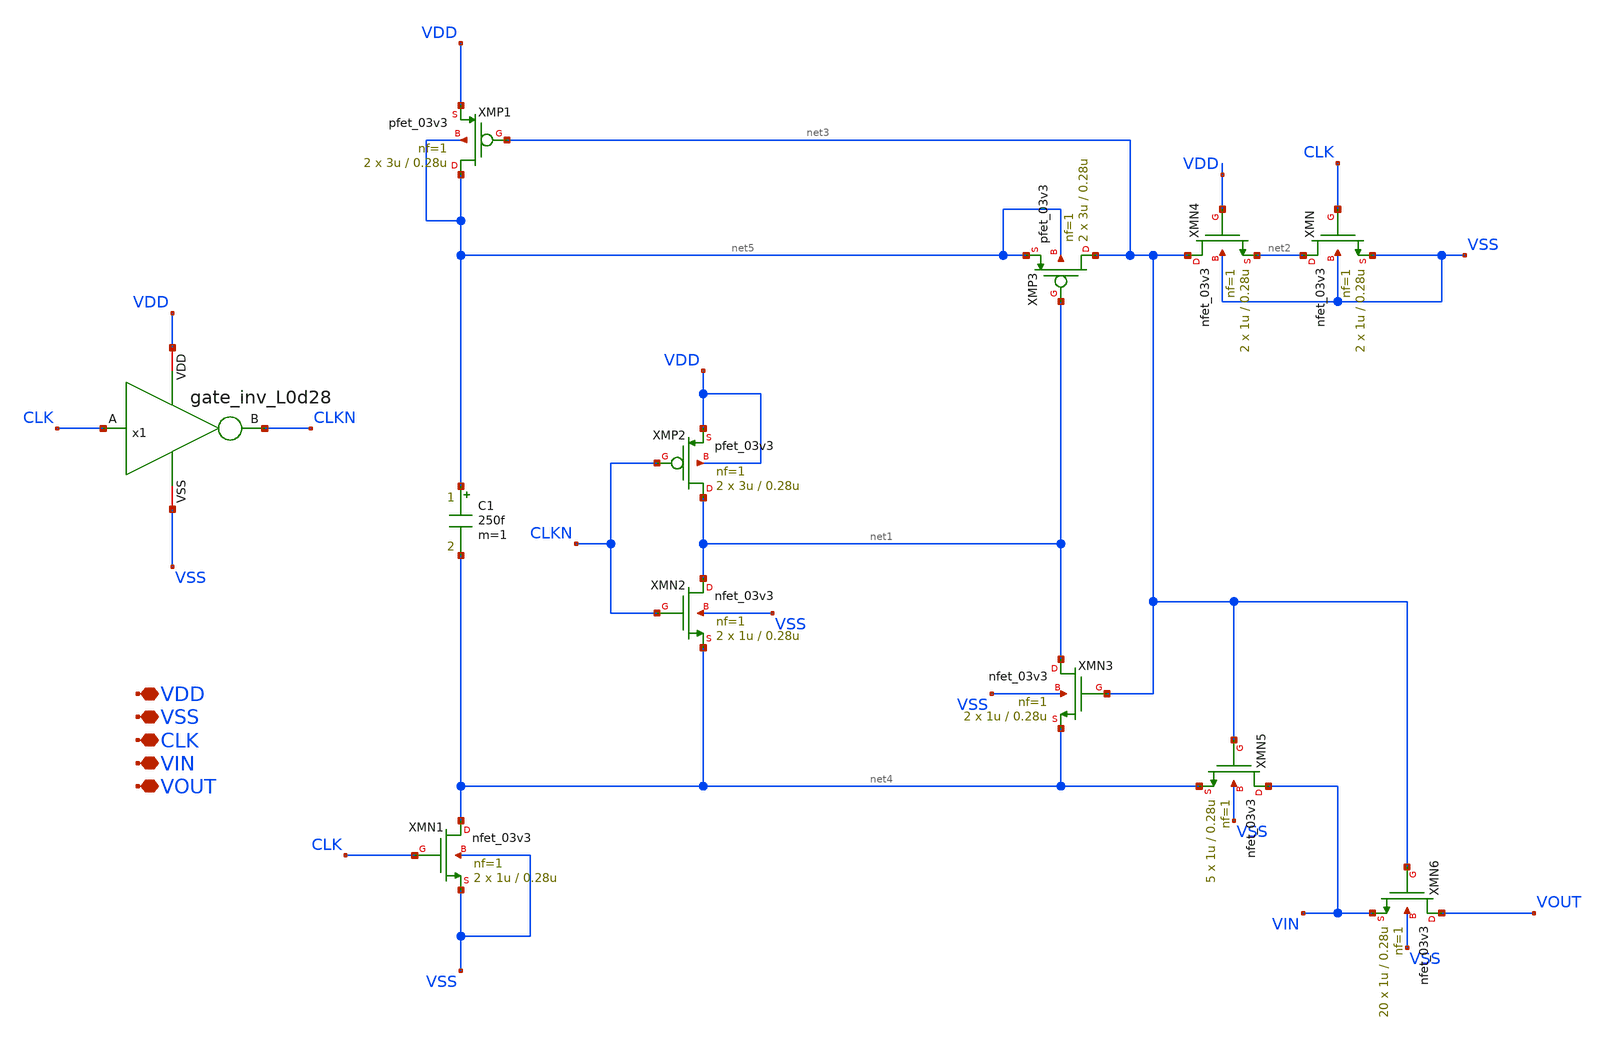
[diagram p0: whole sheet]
** sch_path: designs/sar_adc/samplehold/samplehold/xschem/samplehold.sch
**.subckt samplehold CLK VSS VDD VOUT VIN
*.iopin CLK
*.iopin VSS
*.iopin VDD
*.iopin VOUT
*.iopin VIN
C1 net5 net4 250f m=1
XMN net2 CLK VSS VSS nfet_03v3 L=0.28u W=1u nf=1 ad='int((nf+1)/2) * W/nf * 0.18u' as='int((nf+2)/2) * W/nf * 0.18u'
+ pd='2*int((nf+1)/2) * (W/nf + 0.18u)' ps='2*int((nf+2)/2) * (W/nf + 0.18u)' nrd='0.18u / W' nrs='0.18u / W'
+ sa=0 sb=0 sd=0 m=2
XMP1 net5 net3 VDD net5 pfet_03v3 L=0.28u W=3u nf=1 ad='int((nf+1)/2) * W/nf * 0.18u' as='int((nf+2)/2) * W/nf * 0.18u'
+ pd='2*int((nf+1)/2) * (W/nf + 0.18u)' ps='2*int((nf+2)/2) * (W/nf + 0.18u)' nrd='0.18u / W' nrs='0.18u / W'
+ sa=0 sb=0 sd=0 m=2
XMN1 net4 CLK VSS VSS nfet_03v3 L=0.28u W=1u nf=1 ad='int((nf+1)/2) * W/nf * 0.18u' as='int((nf+2)/2) * W/nf * 0.18u'
+ pd='2*int((nf+1)/2) * (W/nf + 0.18u)' ps='2*int((nf+2)/2) * (W/nf + 0.18u)' nrd='0.18u / W' nrs='0.18u / W'
+ sa=0 sb=0 sd=0 m=2
XMP2 net1 CLKN VDD VDD pfet_03v3 L=0.28u W=3u nf=1 ad='int((nf+1)/2) * W/nf * 0.18u' as='int((nf+2)/2) * W/nf * 0.18u'
+ pd='2*int((nf+1)/2) * (W/nf + 0.18u)' ps='2*int((nf+2)/2) * (W/nf + 0.18u)' nrd='0.18u / W' nrs='0.18u / W'
+ sa=0 sb=0 sd=0 m=2
XMN2 net1 CLKN net4 VSS nfet_03v3 L=0.28u W=1u nf=1 ad='int((nf+1)/2) * W/nf * 0.18u' as='int((nf+2)/2) * W/nf * 0.18u'
+ pd='2*int((nf+1)/2) * (W/nf + 0.18u)' ps='2*int((nf+2)/2) * (W/nf + 0.18u)' nrd='0.18u / W' nrs='0.18u / W'
+ sa=0 sb=0 sd=0 m=2
XMN3 net1 net3 net4 VSS nfet_03v3 L=0.28u W=1u nf=1 ad='int((nf+1)/2) * W/nf * 0.18u' as='int((nf+2)/2) * W/nf * 0.18u'
+ pd='2*int((nf+1)/2) * (W/nf + 0.18u)' ps='2*int((nf+2)/2) * (W/nf + 0.18u)' nrd='0.18u / W' nrs='0.18u / W'
+ sa=0 sb=0 sd=0 m=2
XMP3 net3 net1 net5 net5 pfet_03v3 L=0.28u W=3u nf=1 ad='int((nf+1)/2) * W/nf * 0.18u' as='int((nf+2)/2) * W/nf * 0.18u'
+ pd='2*int((nf+1)/2) * (W/nf + 0.18u)' ps='2*int((nf+2)/2) * (W/nf + 0.18u)' nrd='0.18u / W' nrs='0.18u / W'
+ sa=0 sb=0 sd=0 m=2
XMN4 net3 VDD net2 VSS nfet_03v3 L=0.28u W=1u nf=1 ad='int((nf+1)/2) * W/nf * 0.18u' as='int((nf+2)/2) * W/nf * 0.18u'
+ pd='2*int((nf+1)/2) * (W/nf + 0.18u)' ps='2*int((nf+2)/2) * (W/nf + 0.18u)' nrd='0.18u / W' nrs='0.18u / W'
+ sa=0 sb=0 sd=0 m=2
XMN5 VIN net3 net4 VSS nfet_03v3 L=0.28u W=1u nf=1 ad='int((nf+1)/2) * W/nf * 0.18u' as='int((nf+2)/2) * W/nf * 0.18u'
+ pd='2*int((nf+1)/2) * (W/nf + 0.18u)' ps='2*int((nf+2)/2) * (W/nf + 0.18u)' nrd='0.18u / W' nrs='0.18u / W'
+ sa=0 sb=0 sd=0 m=5
XMN6 VOUT net3 VIN VSS nfet_03v3 L=0.28u W=1u nf=1 ad='int((nf+1)/2) * W/nf * 0.18u' as='int((nf+2)/2) * W/nf * 0.18u'
+ pd='2*int((nf+1)/2) * (W/nf + 0.18u)' ps='2*int((nf+2)/2) * (W/nf + 0.18u)' nrd='0.18u / W' nrs='0.18u / W'
+ sa=0 sb=0 sd=0 m=20
x1 VDD CLKN CLK VSS gate_inv_L0d28
**.ends

* expanding   symbol:  sar_adc/samplehold/gate_inv_L0d28/xschem/gate_inv_L0d28.sym # of pins=4
** sym_path: sar_adc/samplehold/gate_inv_L0d28/xschem/gate_inv_L0d28.sym
** sch_path: sar_adc/samplehold/gate_inv_L0d28/xschem/gate_inv_L0d28.sch
.subckt gate_inv_L0d28 VDD B A VSS
*.opin B
*.ipin A
*.iopin VDD
*.iopin VSS
XMN B A VSS VSS nfet_03v3 L=0.28u W=1u nf=1 ad='int((nf+1)/2) * W/nf * 0.18u' as='int((nf+2)/2) * W/nf * 0.18u'
+ pd='2*int((nf+1)/2) * (W/nf + 0.18u)' ps='2*int((nf+2)/2) * (W/nf + 0.18u)' nrd='0.18u / W' nrs='0.18u / W'
+ sa=0 sb=0 sd=0 m=2
XMP B A VDD VDD pfet_03v3 L=0.28u W=3u nf=1 ad='int((nf+1)/2) * W/nf * 0.18u' as='int((nf+2)/2) * W/nf * 0.18u'
+ pd='2*int((nf+1)/2) * (W/nf + 0.18u)' ps='2*int((nf+2)/2) * (W/nf + 0.18u)' nrd='0.18u / W' nrs='0.18u / W'
+ sa=0 sb=0 sd=0 m=2
.ends

.end
